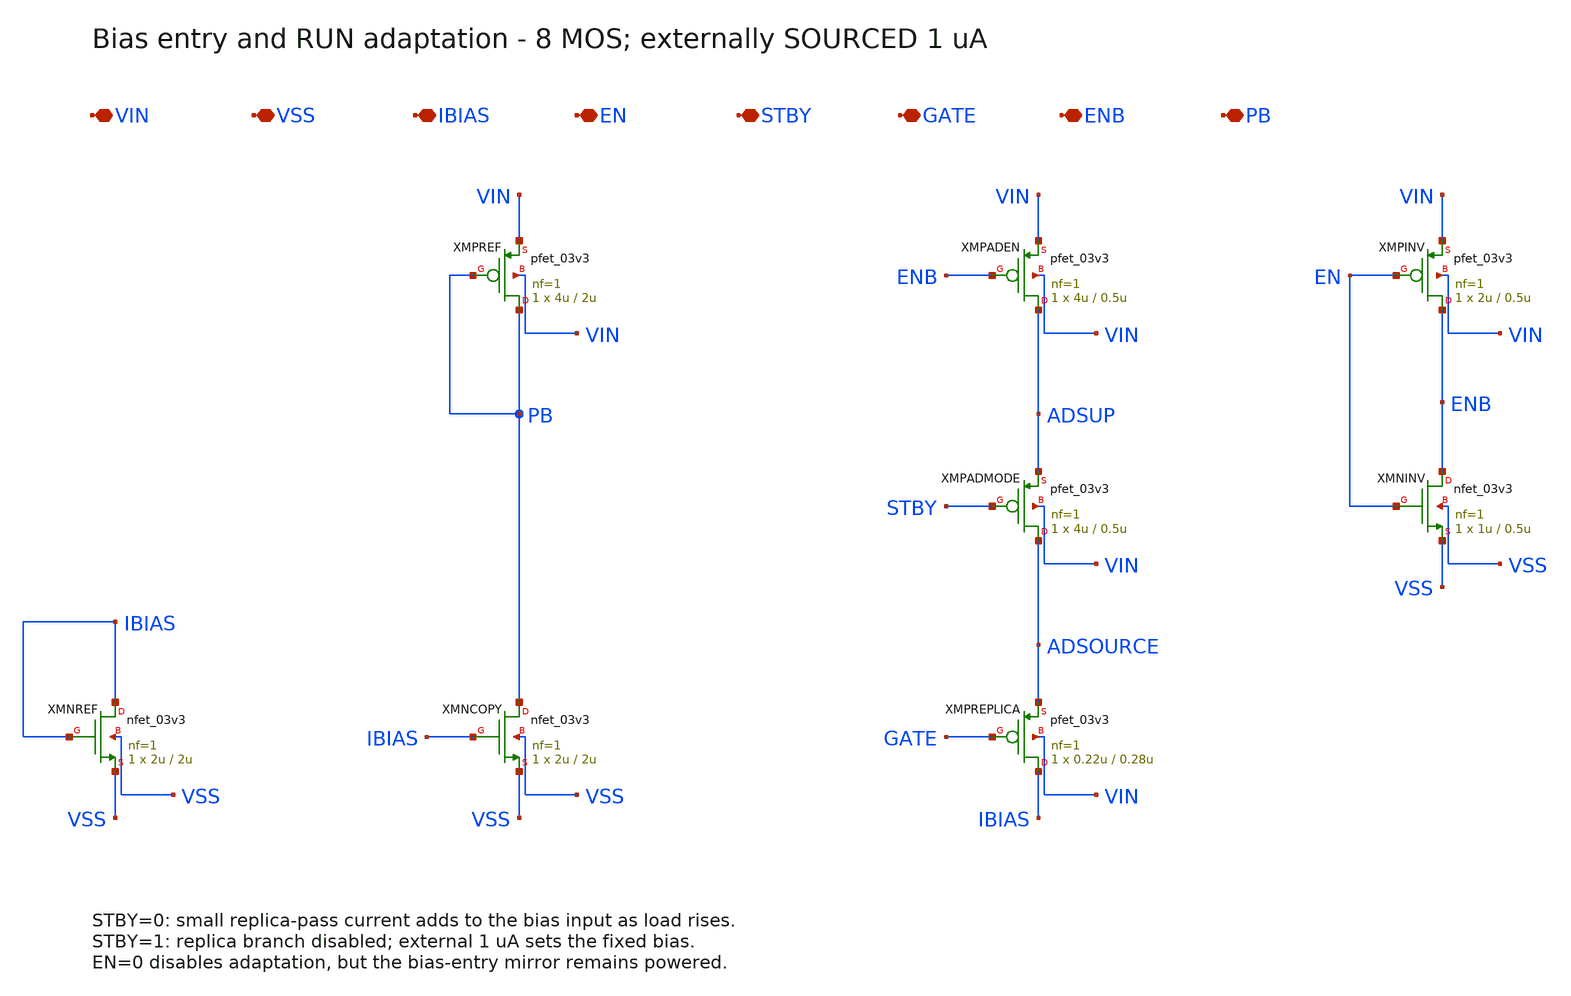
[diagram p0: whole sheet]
** sch_path: schematics/ldo_bias.sch
**.subckt ldo_bias VIN VSS IBIAS EN STBY GATE ENB PB
*.iopin VIN
*.iopin VSS
*.iopin IBIAS
*.iopin EN
*.iopin STBY
*.iopin GATE
*.iopin ENB
*.iopin PB
XMNREF IBIAS IBIAS VSS VSS nfet_03v3 L=2u W=2u nf=1 ad='int((nf+1)/2)*W/nf*0.18u' as='int((nf+2)/2)*W/nf*0.18u'
+ pd='2*int((nf+1)/2)*(W/nf+0.18u)' ps='2*int((nf+2)/2)*(W/nf+0.18u)' nrd='0.18u/W' nrs='0.18u/W' sa=0
+ sb=0 sd=0 m=1 par=1
XMNCOPY PB IBIAS VSS VSS nfet_03v3 L=2u W=2u nf=1 ad='int((nf+1)/2)*W/nf*0.18u' as='int((nf+2)/2)*W/nf*0.18u'
+ pd='2*int((nf+1)/2)*(W/nf+0.18u)' ps='2*int((nf+2)/2)*(W/nf+0.18u)' nrd='0.18u/W' nrs='0.18u/W' sa=0
+ sb=0 sd=0 m=1 par=1
XMPREF PB PB VIN VIN pfet_03v3 L=2u W=4u nf=1 ad='int((nf+1)/2)*W/nf*0.18u' as='int((nf+2)/2)*W/nf*0.18u'
+ pd='2*int((nf+1)/2)*(W/nf+0.18u)' ps='2*int((nf+2)/2)*(W/nf+0.18u)' nrd='0.18u/W' nrs='0.18u/W' sa=0
+ sb=0 sd=0 m=1 par=1
XMPADEN ADSUP ENB VIN VIN pfet_03v3 L=0.5u W=4u nf=1 ad='int((nf+1)/2)*W/nf*0.18u' as='int((nf+2)/2)*W/nf*0.18u'
+ pd='2*int((nf+1)/2)*(W/nf+0.18u)' ps='2*int((nf+2)/2)*(W/nf+0.18u)' nrd='0.18u/W' nrs='0.18u/W' sa=0
+ sb=0 sd=0 m=1 par=1
XMPADMODE ADSOURCE STBY ADSUP VIN pfet_03v3 L=0.5u W=4u nf=1 ad='int((nf+1)/2)*W/nf*0.18u' as='int((nf+2)/2)*W/nf*0.18u'
+ pd='2*int((nf+1)/2)*(W/nf+0.18u)' ps='2*int((nf+2)/2)*(W/nf+0.18u)' nrd='0.18u/W' nrs='0.18u/W' sa=0
+ sb=0 sd=0 m=1 par=1
XMPREPLICA IBIAS GATE ADSOURCE VIN pfet_03v3 L=0.28u W=0.22u nf=1 ad='int((nf+1)/2)*W/nf*0.18u' as='int((nf+2)/2)*W/nf*0.18u'
+ pd='2*int((nf+1)/2)*(W/nf+0.18u)' ps='2*int((nf+2)/2)*(W/nf+0.18u)' nrd='0.18u/W' nrs='0.18u/W' sa=0
+ sb=0 sd=0 m=1 par=1
XMPINV ENB EN VIN VIN pfet_03v3 L=0.5u W=2u nf=1 ad='int((nf+1)/2)*W/nf*0.18u' as='int((nf+2)/2)*W/nf*0.18u'
+ pd='2*int((nf+1)/2)*(W/nf+0.18u)' ps='2*int((nf+2)/2)*(W/nf+0.18u)' nrd='0.18u/W' nrs='0.18u/W' sa=0
+ sb=0 sd=0 m=1 par=1
XMNINV ENB EN VSS VSS nfet_03v3 L=0.5u W=1u nf=1 ad='int((nf+1)/2)*W/nf*0.18u' as='int((nf+2)/2)*W/nf*0.18u'
+ pd='2*int((nf+1)/2)*(W/nf+0.18u)' ps='2*int((nf+2)/2)*(W/nf+0.18u)' nrd='0.18u/W' nrs='0.18u/W' sa=0
+ sb=0 sd=0 m=1 par=1
**.ends
.end
